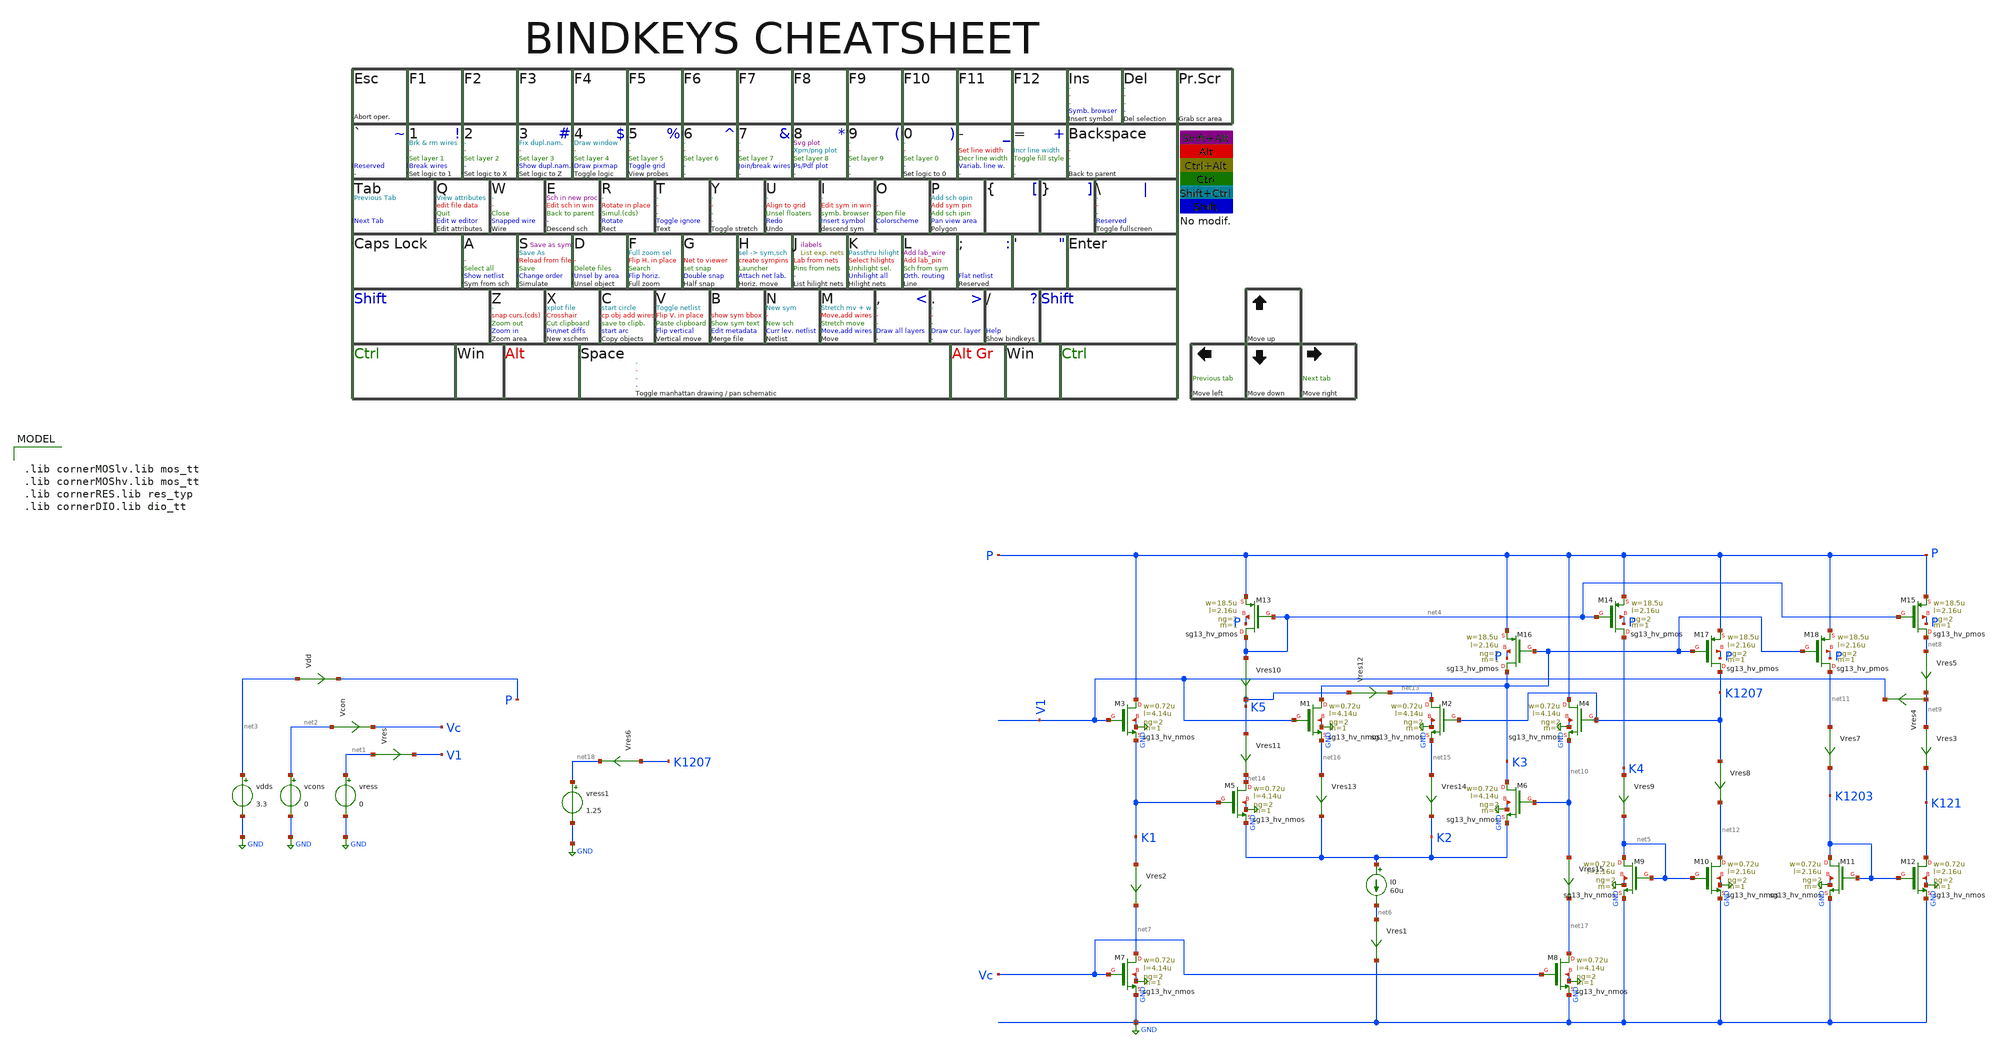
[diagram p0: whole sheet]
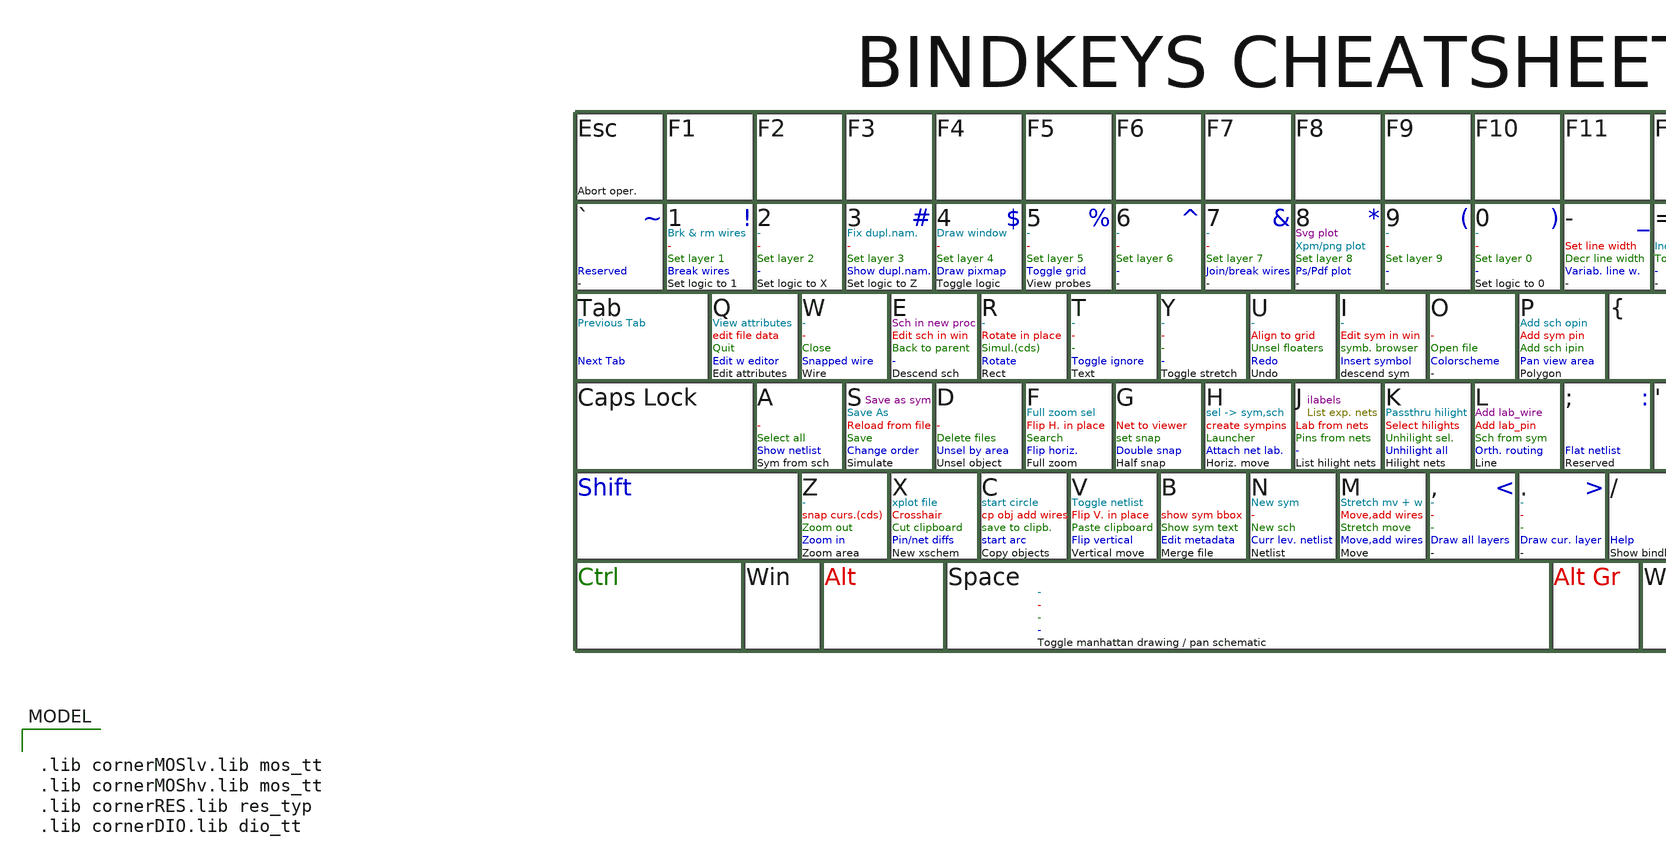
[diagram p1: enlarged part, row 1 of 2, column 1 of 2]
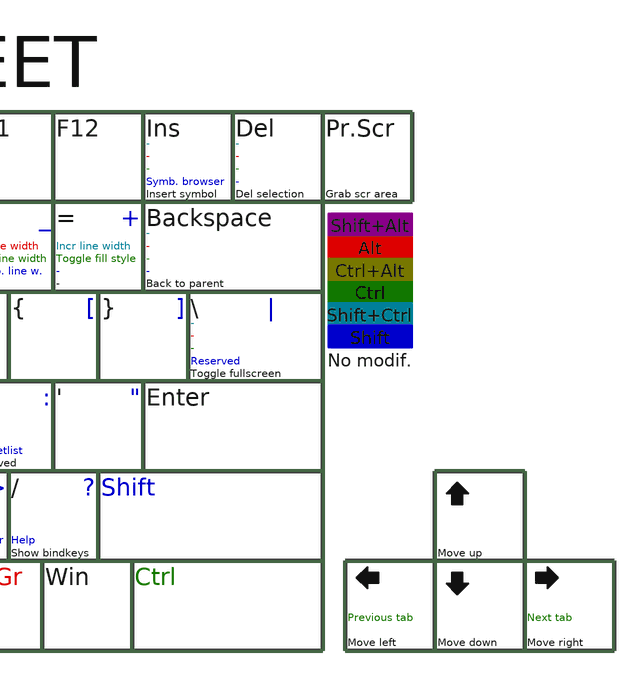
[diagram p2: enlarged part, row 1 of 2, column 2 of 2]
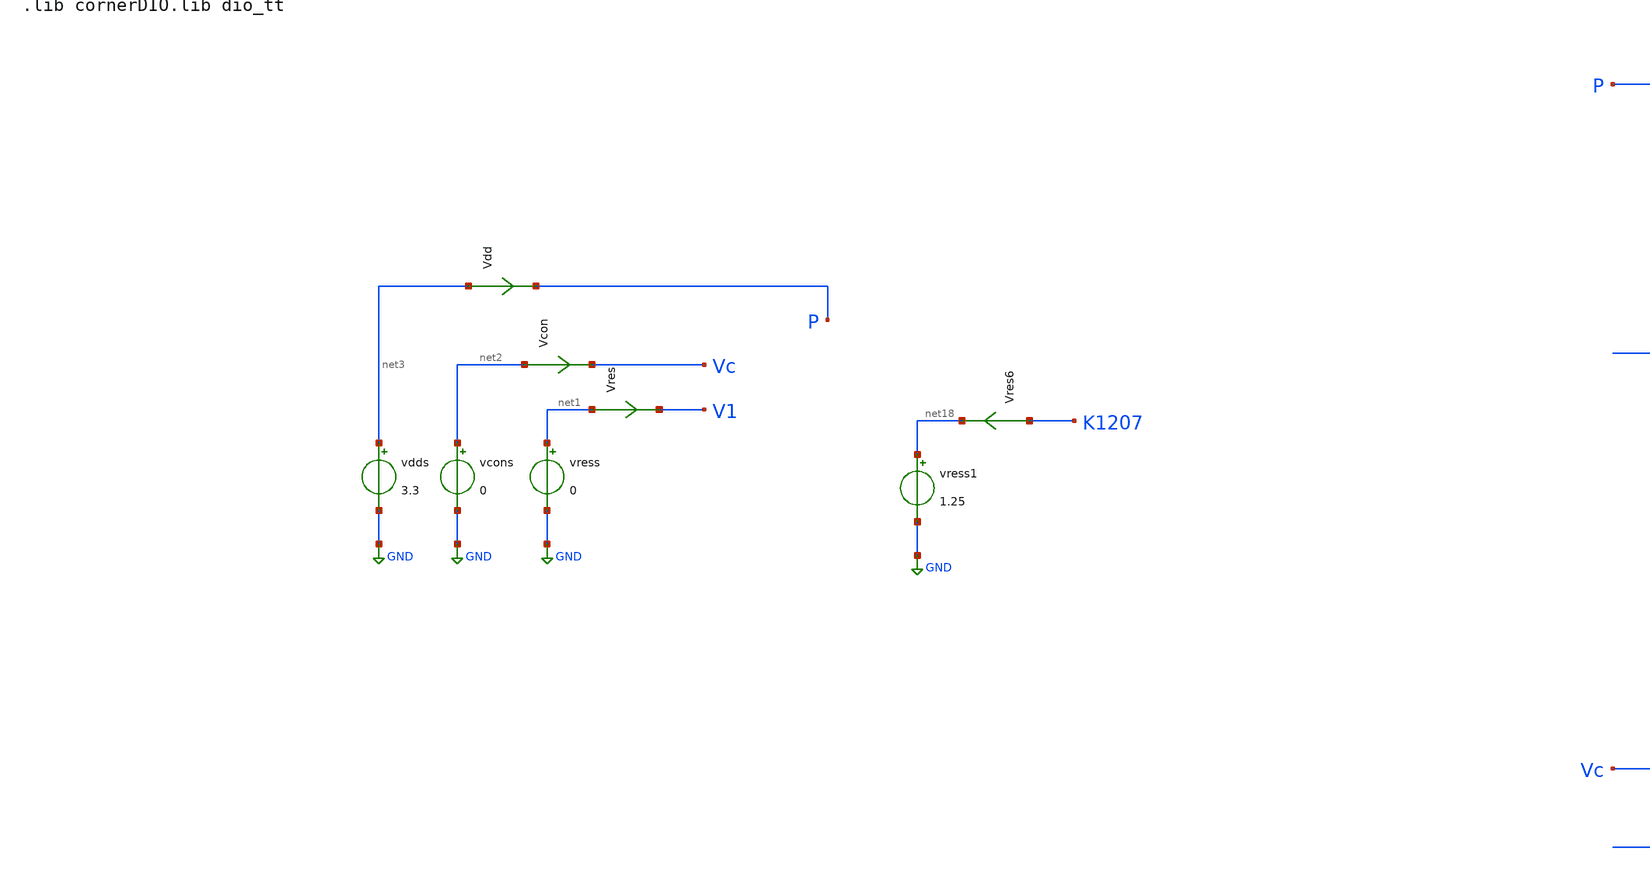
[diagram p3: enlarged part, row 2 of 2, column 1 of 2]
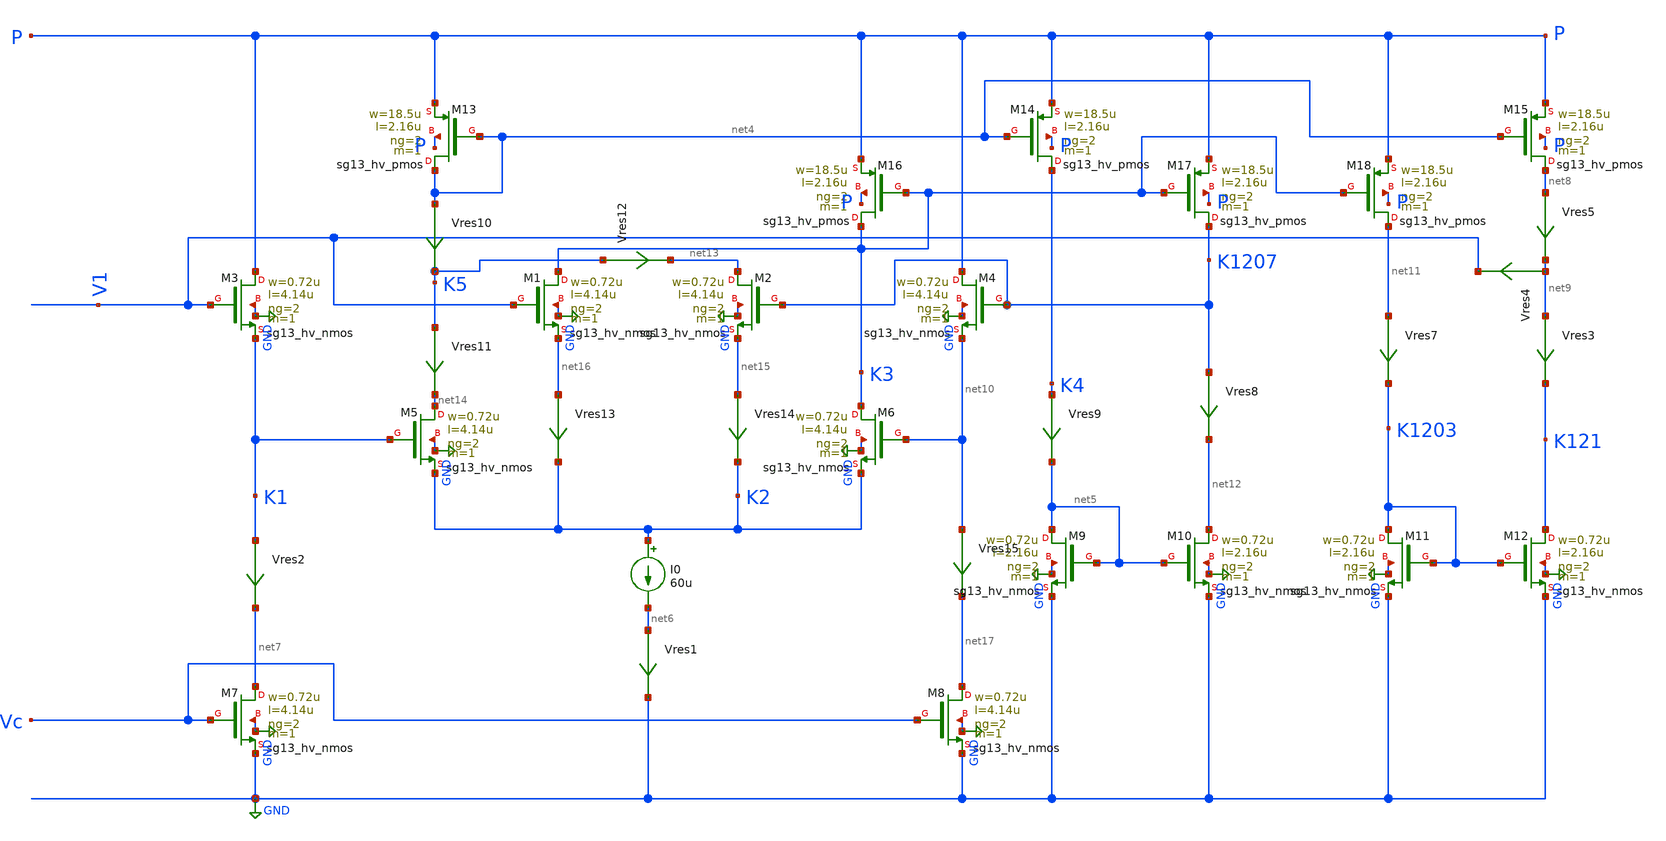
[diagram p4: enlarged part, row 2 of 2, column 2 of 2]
** sch_path: macros/heichips26_analog_project/macros/yadav/testbenches/xschem/plm.sch
**.subckt plm
Vres net1 V1 0
.save i(vres)
vress net1 GND 0
vcons net2 GND 0
vdds net3 GND 3.3
Vcon net2 Vc 0
.save i(vcon)
Vdd net3 P 0
.save i(vdd)
XM3 P V1 K1 GND sg13_hv_nmos w=0.72u l=4.14u ng=2 m=1 mm_ok=1
XM13 net4 net4 P P sg13_hv_pmos w=18.5u l=2.16u ng=2 m=1 mm_ok=1
XM1 K3 V1 net16 GND sg13_hv_nmos w=0.72u l=4.14u ng=2 m=1 mm_ok=1
XM5 net14 K1 K2 GND sg13_hv_nmos w=0.72u l=4.14u ng=2 m=1 mm_ok=1
XM2 net13 K1207 net15 GND sg13_hv_nmos w=0.72u l=4.14u ng=2 m=1 mm_ok=1
XM16 K3 K3 P P sg13_hv_pmos w=18.5u l=2.16u ng=2 m=1 mm_ok=1
XM7 net7 Vc GND GND sg13_hv_nmos w=0.72u l=4.14u ng=2 m=1 mm_ok=1
XM6 K3 net10 K2 GND sg13_hv_nmos w=0.72u l=4.14u ng=2 m=1 mm_ok=1
XM14 K4 net4 P P sg13_hv_pmos w=18.5u l=2.16u ng=2 m=1 mm_ok=1
XM8 net17 Vc GND GND sg13_hv_nmos w=0.72u l=4.14u ng=2 m=1 mm_ok=1
XM4 P K1207 net10 GND sg13_hv_nmos w=0.72u l=4.14u ng=2 m=1 mm_ok=1
XM9 net5 net5 GND GND sg13_hv_nmos w=0.72u l=2.16u ng=2 m=1 mm_ok=1
XM10 net12 net5 GND GND sg13_hv_nmos w=0.72u l=2.16u ng=2 m=1 mm_ok=1
XM17 K1207 K3 P P sg13_hv_pmos w=18.5u l=2.16u ng=2 m=1 mm_ok=1
XM18 net11 K3 P P sg13_hv_pmos w=18.5u l=2.16u ng=2 m=1 mm_ok=1
XM11 K1203 K1203 GND GND sg13_hv_nmos w=0.72u l=2.16u ng=2 m=1 mm_ok=1
XM12 K121 K1203 GND GND sg13_hv_nmos w=0.72u l=2.16u ng=2 m=1 mm_ok=1
XM15 net8 net4 P P sg13_hv_pmos w=18.5u l=2.16u ng=2 m=1 mm_ok=1
I0 K2 net6 60u
Vres1 net6 GND 0
.save i(vres1)
Vres2 K1 net7 0
.save i(vres2)
Vres3 net9 K121 0
.save i(vres3)
Vres4 net9 V1 0
.save i(vres4)
Vres5 net8 net9 0
.save i(vres5)
Vres7 net11 K1203 0
.save i(vres7)
Vres8 K1207 net12 0
.save i(vres8)
Vres9 K4 net5 0
.save i(vres9)
Vres10 net4 K5 0
.save i(vres10)
Vres11 K5 net14 0
.save i(vres11)
Vres12 K5 net13 0
.save i(vres12)
Vres13 net16 K2 0
.save i(vres13)
Vres14 net15 K2 0
.save i(vres14)
Vres15 net10 net17 0
.save i(vres15)
Vres6 K1207 net18 0
.save i(vres6)
vress1 net18 GND 1.25
**** begin user architecture code


* .include ../../../netlist/pex/inverter_magic_pex_3.spice
.param temp=27
.options savecurrents klu method=gear reltol=1e-3 abstol=1e-15 gmin=1e-15 rshunt=1e10
.control
save all
set appendwrite

* DC Sweep
* dc vcon 1 1.5 1m
* remzerovec

* plot v(vres)/i(Vres)
*plot v(VStage1)
*plot v(VStage2)



let vcc = 0.4
repeat 5
  alter vcons $&vcc

  * DC Sweep
  dc vress 0.3 3.3 1m
  remzerovec
  let vcc = vcc + 0.15
end
set appendwrite

*plot dc1.v(V1)/(dc1.i(Vres)) dc2.v(V1)/(dc2.i(Vres)) dc3.v(V1)/(dc3.i(Vres))
*+ dc4.v(V1)/(dc4.i(Vres)) dc5.v(V1)/(dc5.i(Vres))

*plot dc1.v(V1)/(dc1.i(Vres6)) dc2.v(V1)/(dc2.i(Vres6)) dc3.v(V1)/(dc3.i(Vres6))
*+ dc4.v(V1)/(dc4.i(Vres6)) dc5.v(V1)/(dc5.i(Vres6))

plot (dc1.i(Vres)) (dc2.i(Vres)) (dc3.i(Vres)) (dc4.i(Vres)) (dc5.i(Vres))

plot (dc1.i(Vres6)) (dc2.i(Vres6)) (dc3.i(Vres6)) (dc4.i(Vres6))  (dc5.i(Vres6))


* Write Data
unset appendwrite
set wr_vecnames
set wr_singlescale

*quit
.endc



.lib cornerMOSlv.lib mos_tt
.lib cornerMOShv.lib mos_tt
.lib cornerRES.lib res_typ
.lib cornerDIO.lib dio_tt

**** end user architecture code
**.ends
.GLOBAL GND
.end
